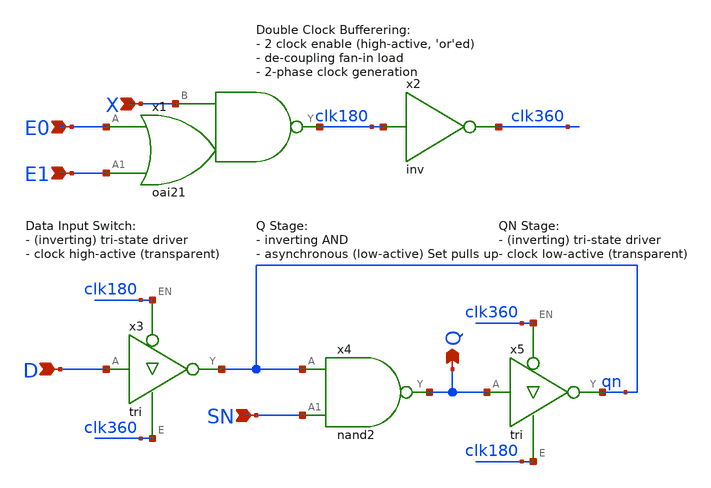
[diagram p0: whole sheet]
** sch_path: Sources/crafted/LATEESP.sch
**.subckt LATEESP X D Q E0 E1 SN
*.ipin X
*.ipin D
*.opin Q
*.ipin E0
*.ipin E1
*.ipin SN
x2 clk180 clk360 VDD GND inv Wmin=1.5u Lmin=1u g=2 m=1
x3 D clk180 clk360 qn VDD GND tri Wmin=1.5u Lmin=1u g=2 m=1
x5 Q clk360 clk180 qn VDD GND tri Wmin=1.5u Lmin=1u g=2 m=1
x1 E0 E1 clk180 X VDD GND oai21 Wmin=1.5u Lmin=1u g=2 m=1
x4 Q qn SN VDD GND nand2 Wmin=1.5u Lmin=1u g=2 m=1
**.ends
.end
